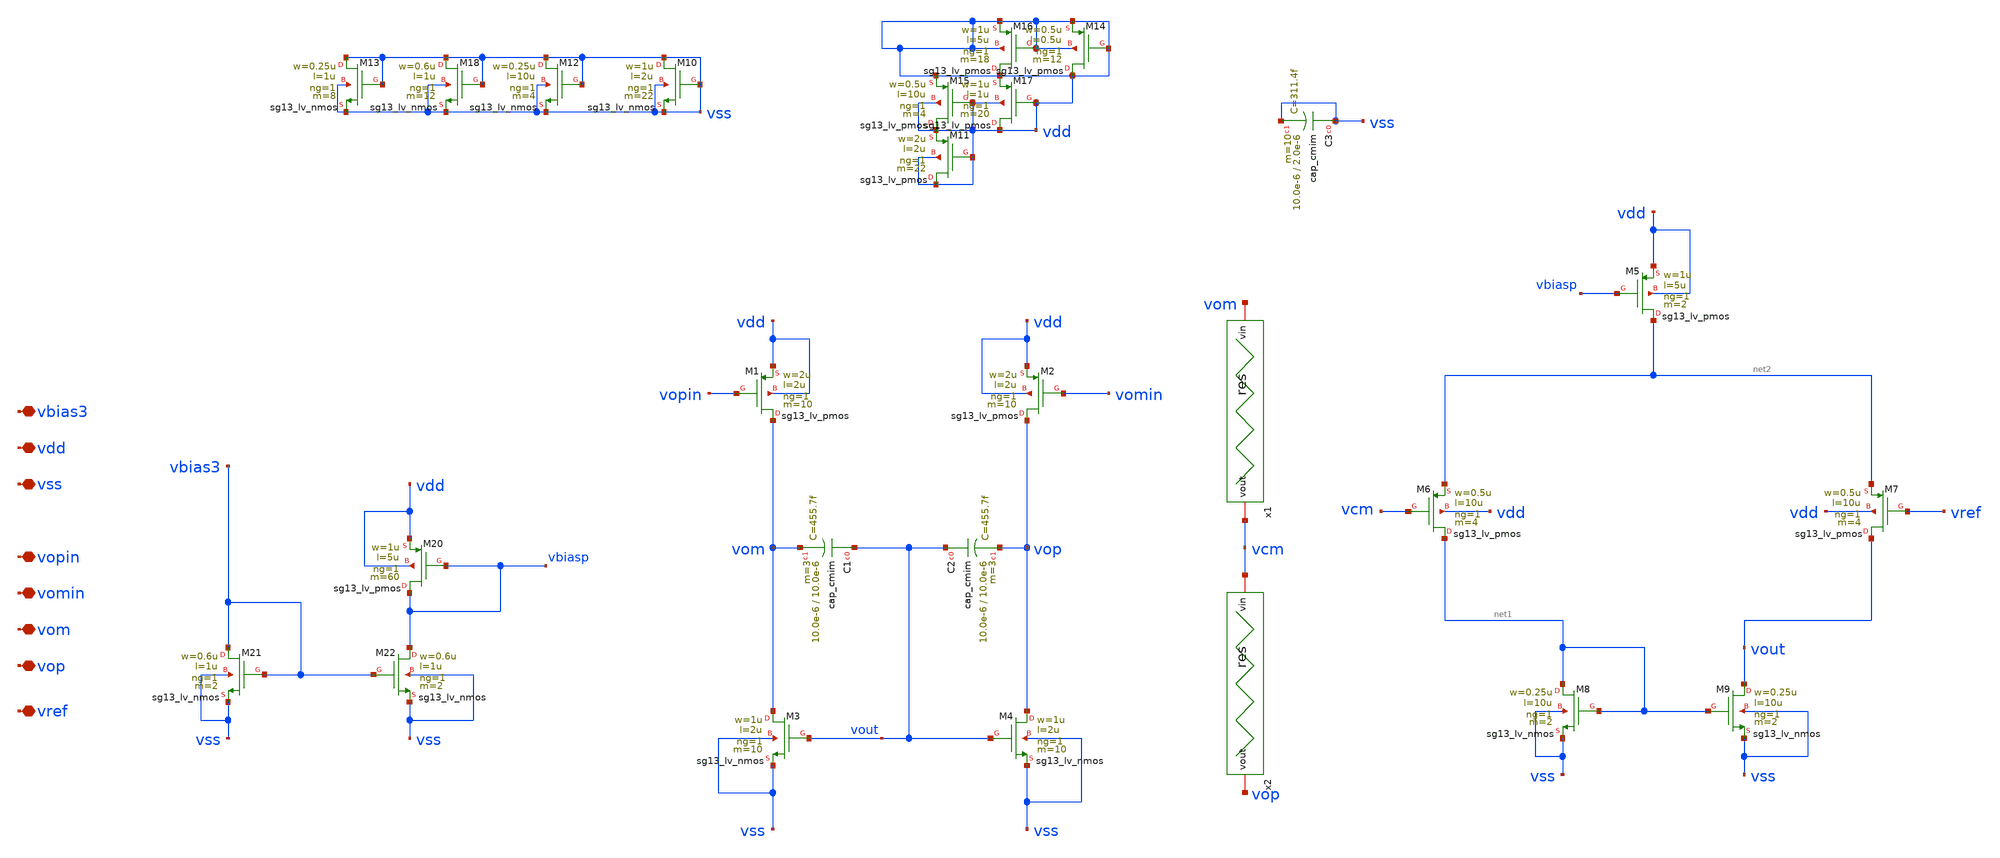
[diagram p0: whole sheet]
** sch_path: LVS/Unic_cass_final_design_lvs/Simulations/Opamp_design/Src/common_source_stage.sch
**.subckt common_source_stage vbias3 vdd vss vopin vomin vom vop vref
*.iopin vbias3
*.iopin vdd
*.iopin vss
*.iopin vopin
*.iopin vomin
*.iopin vom
*.iopin vop
*.iopin vref
XM20 vbiasp vbiasp vdd vdd sg13_lv_pmos w=1u l=5u ng=1 m=60 mm_ok=1
XM21 vbias3 vbias3 vss vss sg13_lv_nmos w=0.6u l=1u ng=1 m=2 mm_ok=1
XM22 vbiasp vbias3 vss vss sg13_lv_nmos w=0.6u l=1u ng=1 m=2 mm_ok=1
XM1 vom vopin vdd vdd sg13_lv_pmos w=2u l=2u ng=1 m=10 mm_ok=1
XM2 vop vomin vdd vdd sg13_lv_pmos w=2u l=2u ng=1 m=10 mm_ok=1
XM3 vom vout vss vss sg13_lv_nmos w=1u l=2u ng=1 m=10 mm_ok=1
XM4 vop vout vss vss sg13_lv_nmos w=1u l=2u ng=1 m=10 mm_ok=1
XM5 net2 vbiasp vdd vdd sg13_lv_pmos w=1u l=5u ng=1 m=2 mm_ok=1
XM6 net1 vcm net2 vdd sg13_lv_pmos w=0.5u l=10u ng=1 m=4 mm_ok=1
XM7 vout vref net2 vdd sg13_lv_pmos w=0.5u l=10u ng=1 m=4 mm_ok=1
XM8 net1 net1 vss vss sg13_lv_nmos w=0.25u l=10u ng=1 m=2 mm_ok=1
XM9 vout net1 vss vss sg13_lv_nmos w=0.25u l=10u ng=1 m=2 mm_ok=1
XC1 vout vom cap_cmim w=10.0e-6 l=10.0e-6 m=3 mm_ok=1
XC2 vout vop cap_cmim w=10.0e-6 l=10.0e-6 m=3 mm_ok=1
XM10 vss vss vss vss sg13_lv_nmos w=1u l=2u ng=1 m=22 mm_ok=1
XM12 vss vss vss vss sg13_lv_nmos w=0.25u l=10u ng=1 m=4 mm_ok=1
XM13 vss vss vss vss sg13_lv_nmos w=0.25u l=1u ng=1 m=8 mm_ok=1
XM14 vdd vdd vdd vdd sg13_lv_pmos w=0.5u l=0.5u ng=1 m=12 mm_ok=1
XM15 vdd vdd vdd vdd sg13_lv_pmos w=0.5u l=10u ng=1 m=4 mm_ok=1
XM17 vdd vdd vdd vdd sg13_lv_pmos w=1u l=1u ng=1 m=20 mm_ok=1
XM18 vss vss vss vss sg13_lv_nmos w=0.6u l=1u ng=1 m=12 mm_ok=1
XM16 vdd vdd vdd vdd sg13_lv_pmos w=1u l=5u ng=1 m=18 mm_ok=1
XM11 vdd vdd vdd vdd sg13_lv_pmos w=2u l=2u ng=1 m=22 mm_ok=1
XC3 vss vss cap_cmim w=10.0e-6 l=2.0e-6 m=10 mm_ok=1
x1 vom vcm res
x2 vcm vop res
**.ends
.end
